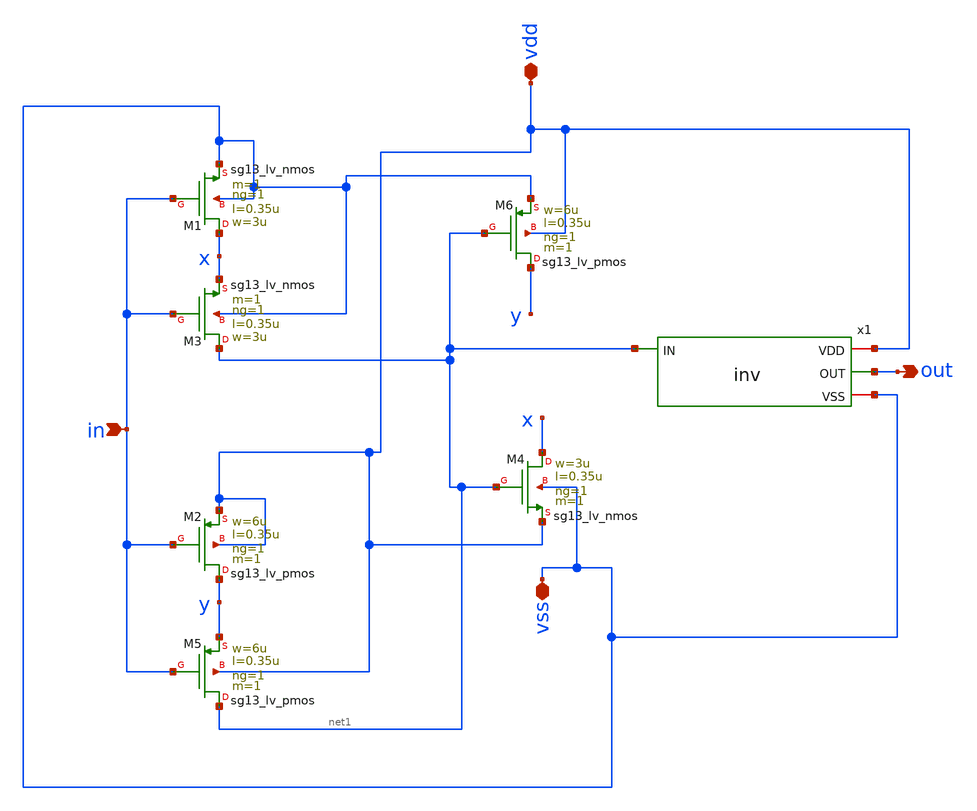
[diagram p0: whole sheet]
** sch_path: macros/heichips26_chronosense/schematic/xschem/schmitt.sch
* macros/heichips26_chronosense/schematic/xschem/inv.sch:
* Copyright 2023 IHP PDK Authors
* Licensed under the Apache License, Version 2.0 (the "License");
**.subckt schmitt in vdd vss out
*.ipin in
*.iopin vdd
*.iopin vss
*.opin out
XM1 x in vss vss sg13_lv_nmos w=3u l=0.35u ng=1 m=1 mm_ok=1
XM2 y in vdd vdd sg13_lv_pmos w=6u l=0.35u ng=1 m=1 mm_ok=1
XM3 net1 in x vss sg13_lv_nmos w=3u l=0.35u ng=1 m=1 mm_ok=1
XM4 x net1 vdd vss sg13_lv_nmos w=3u l=0.35u ng=1 m=1 mm_ok=1
XM5 net1 in y vdd sg13_lv_pmos w=6u l=0.35u ng=1 m=1 mm_ok=1
XM6 y net1 vss vdd sg13_lv_pmos w=6u l=0.35u ng=1 m=1 mm_ok=1
x1 vdd net1 out vss inv
**.ends

* expanding   symbol:  inv.sym # of pins=4
** sym_path: macros/heichips26_chronosense/schematic/xschem/inv.sym
** sch_path: macros/heichips26_chronosense/schematic/xschem/inv.sch
.subckt inv VDD IN OUT VSS
*.ipin in
*.opin out
*.iopin vdd
*.iopin vss
XM1 out in vdd vdd sg13_lv_pmos w=2u l=0.35u ng=1 m=1 mm_ok=1
XM2 out in vss vss sg13_lv_nmos w=1u l=0.35u ng=1 m=1 mm_ok=1
.ends

.end
